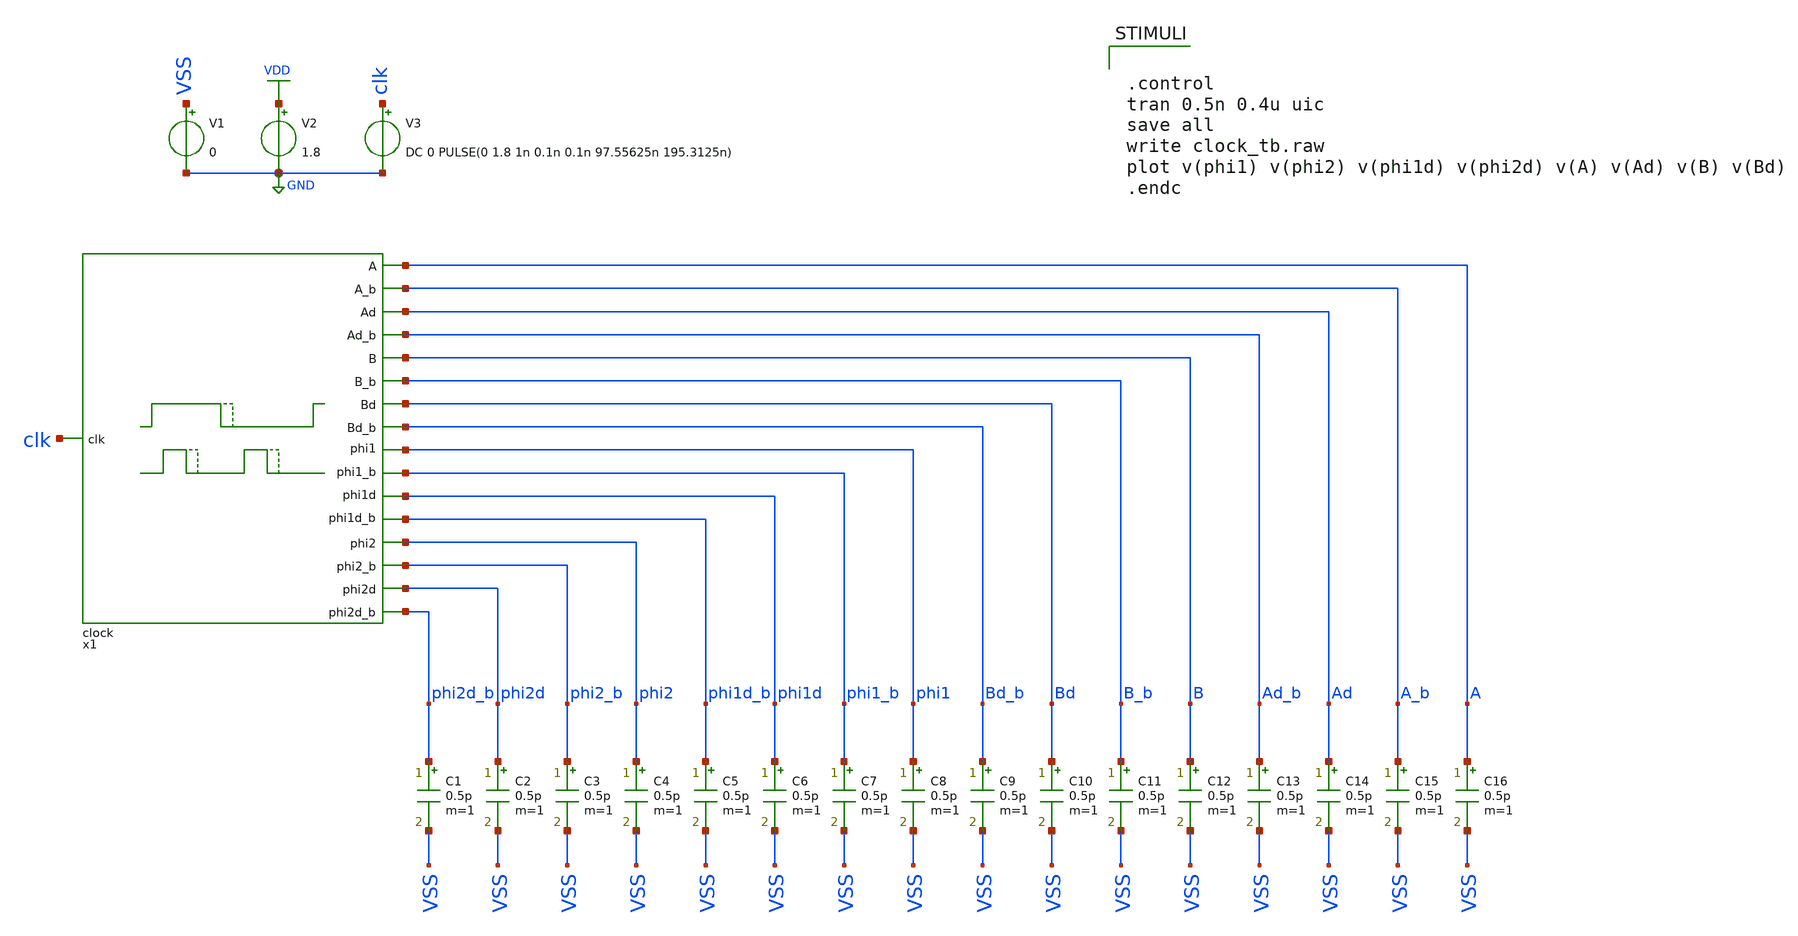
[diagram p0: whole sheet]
** sch_path: verification/schematic_sim/clock_tb.sch
**.subckt clock_tb
x1 A A_b Ad Ad_b Bd_b Bd B_b B phi2 phi2_b phi2d clk phi2d_b phi1d_b phi1d phi1_b phi1 VDD VSS clock
V1 VSS GND 0
V2 VDD GND 1.8
V3 clk GND DC 0 PULSE(0 1.8 1n 0.1n 0.1n 97.55625n 195.3125n)
C1 phi2d_b VSS 0.5p m=1
C2 phi2d VSS 0.5p m=1
C3 phi2_b VSS 0.5p m=1
C4 phi2 VSS 0.5p m=1
C5 phi1d_b VSS 0.5p m=1
C6 phi1d VSS 0.5p m=1
C7 phi1_b VSS 0.5p m=1
C8 phi1 VSS 0.5p m=1
C9 Bd_b VSS 0.5p m=1
C10 Bd VSS 0.5p m=1
C11 B_b VSS 0.5p m=1
C12 B VSS 0.5p m=1
C13 Ad_b VSS 0.5p m=1
C14 Ad VSS 0.5p m=1
C15 A_b VSS 0.5p m=1
C16 A VSS 0.5p m=1
**** begin user architecture code

** opencircuitdesign pdks install
.lib /farmshare/home/classes/ee/372/PDKs/open_pdks_1.0.310/sky130/sky130A/libs.tech/ngspice/sky130.lib.spice tt
.inc /farmshare/home/classes/ee/372/PDKs/open_pdks_1.0.310/sky130/sky130A/libs.ref/sky130_fd_sc_hd/spice/sky130_fd_sc_hd.spice



.control
tran 0.5n 0.4u uic
save all
write clock_tb.raw
plot v(phi1) v(phi2) v(phi1d) v(phi2d) v(A) v(Ad) v(B) v(Bd)
.endc


**** end user architecture code
**.ends
.GLOBAL GND
.GLOBAL VDD
.end
